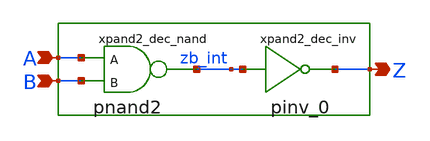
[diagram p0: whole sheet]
** sch_path: sram_2_64_scn4m/and2_dec_0.sch
**.subckt and2_dec_0 A B Z
*.ipin A
*.ipin B
*.opin Z
xpand2_dec_nand A B zb_int vdd gnd pnand2
xpand2_dec_inv zb_int Z vdd gnd pinv_0
**.ends

* expanding   symbol:  pnand2.sym # of pins=3
** sym_path: sram_2_64_scn4m/pnand2.sym
** sch_path: sram_2_64_scn4m/pnand2.sch
.subckt pnand2 A B Z vdd gnd
*.ipin A
*.ipin B
*.opin Z
*.iopin vdd
*.iopin gnd
XMpnand2_nmos1 Z B net1 gnd sky130_fd_pr__nfet_01v8 L=0.4 W=1.6 nf=1 ad='int((nf+1)/2) * W/nf * 0.29'
+ as='int((nf+2)/2) * W/nf * 0.29' pd='2*int((nf+1)/2) * (W/nf + 0.29)' ps='2*int((nf+2)/2) * (W/nf + 0.29)'
+ nrd='0.29 / W' nrs='0.29 / W' sa=0 sb=0 sd=0 mult=1 m=1
XMpnand2_pmos1 Z A vdd vdd sky130_fd_pr__pfet_01v8 L=0.4 W=1.6 nf=1 ad='int((nf+1)/2) * W/nf * 0.29'
+ as='int((nf+2)/2) * W/nf * 0.29' pd='2*int((nf+1)/2) * (W/nf + 0.29)' ps='2*int((nf+2)/2) * (W/nf + 0.29)'
+ nrd='0.29 / W' nrs='0.29 / W' sa=0 sb=0 sd=0 mult=1 m=1
XMpnand2_pmos2 Z B vdd vdd sky130_fd_pr__pfet_01v8 L=0.4 W=1.6 nf=1 ad='int((nf+1)/2) * W/nf * 0.29'
+ as='int((nf+2)/2) * W/nf * 0.29' pd='2*int((nf+1)/2) * (W/nf + 0.29)' ps='2*int((nf+2)/2) * (W/nf + 0.29)'
+ nrd='0.29 / W' nrs='0.29 / W' sa=0 sb=0 sd=0 mult=1 m=1
XMpnand2_nmos2 net1 A gnd gnd sky130_fd_pr__nfet_01v8 L=0.4 W=1.6 nf=1 ad='int((nf+1)/2) * W/nf * 0.29'
+ as='int((nf+2)/2) * W/nf * 0.29' pd='2*int((nf+1)/2) * (W/nf + 0.29)' ps='2*int((nf+2)/2) * (W/nf + 0.29)'
+ nrd='0.29 / W' nrs='0.29 / W' sa=0 sb=0 sd=0 mult=1 m=1
.ends


* expanding   symbol:  pinv_0.sym # of pins=2
** sym_path: sram_2_16_scn4m/pinv_0.sym
** sch_path: sram_2_16_scn4m/pinv_0.sch
.subckt pinv_0 A Z vdd gnd
*.ipin A
*.opin Z
Mpinv_nmos Z A gnd gnd n w=1.6u l=0.4u m=1
Mp_inv_pmos Z A vdd vdd p w=3.2u l=0.4u m=1
.ends

.end
